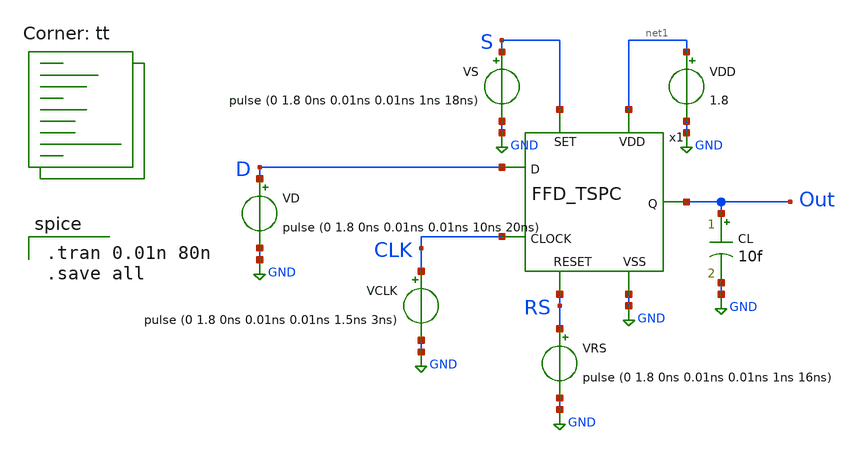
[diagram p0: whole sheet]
** sch_path: FFD_TSPC_tb.sch
**.subckt FFD_TSPC_tb
CL Out GND 10f m=1
VD D GND pulse (0 1.8 0ns 0.01ns 0.01ns 10ns 20ns)
VCLK CLK GND pulse (0 1.8 0ns 0.01ns 0.01ns 1.5ns 3ns)
VRS RS GND pulse (0 1.8 0ns 0.01ns 0.01ns 1ns 16ns)
VS S GND pulse (0 1.8 0ns 0.01ns 0.01ns 1ns 18ns)
VDD net1 GND 1.8
x1 net1 GND S CLK RS D Out FFD_TSPC
**** begin user architecture code
.lib $::SKYWATER_MODELS/sky130.lib.spice tt

.tran 0.01n 80n
.save all

**** end user architecture code
**.ends
.GLOBAL GND
.end
